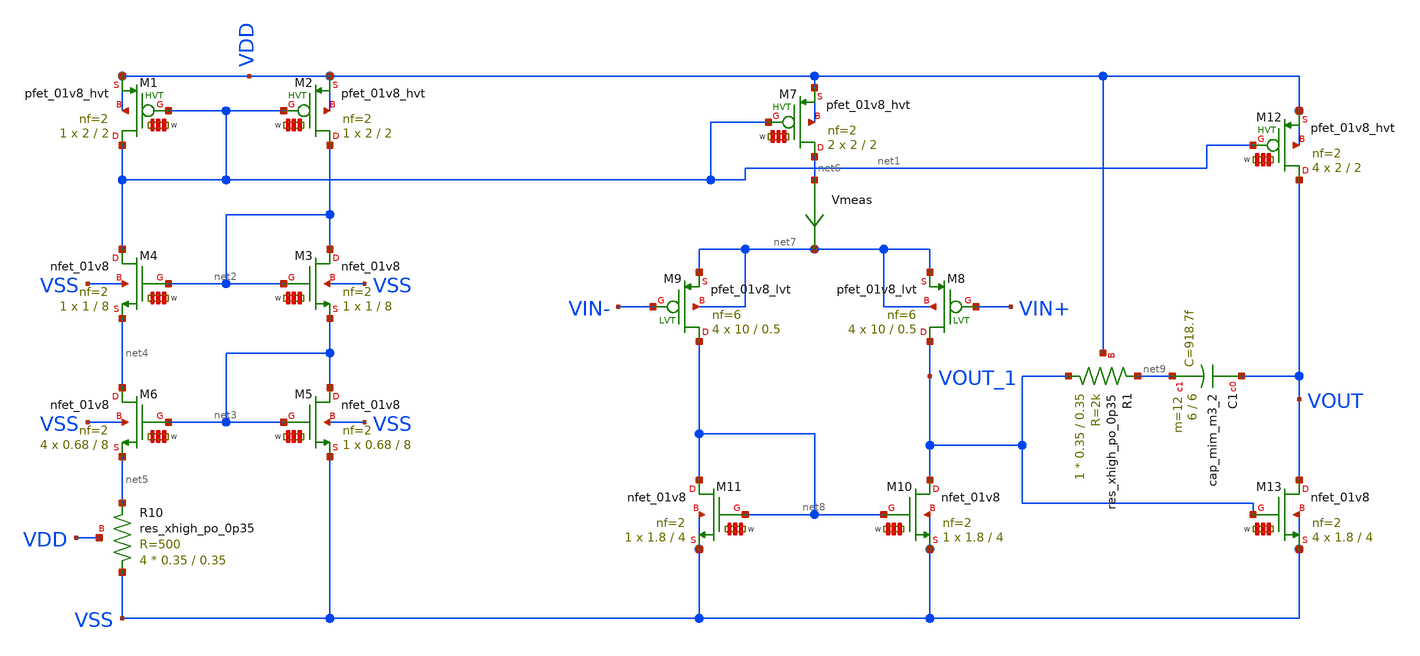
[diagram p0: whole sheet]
** sch_path: my_ip/sky130A/2_stage_op_amp_sky130/op_amp.sch
**.subckt op_amp
XM5 net3 net3 VSS VSS sky130_fd_pr__nfet_01v8 L=8 W='0.68 * 2 ' nf=2 ad='int((2 + 1)/2) * 0.68 / 2 * 0.29'
+ as='int((2 + 2)/2) * 0.68 / 2 * 0.29' pd='2*int((2 + 1)/2) * (0.68 / 2 + 0.29)' ps='2*int((2 + 2)/2) * (0.68 / 2 + 0.29)'
+ nrd='0.29 / 0.68 ' nrs='0.29 / 0.68 ' sa=0 sb=0 sd=0 mult=1 m=1
XM6 net4 net3 net5 VSS sky130_fd_pr__nfet_01v8 L=8 W='0.68 * 2 ' nf=2 ad='int((2 + 1)/2) * 0.68 / 2 * 0.29'
+ as='int((2 + 2)/2) * 0.68 / 2 * 0.29' pd='2*int((2 + 1)/2) * (0.68 / 2 + 0.29)' ps='2*int((2 + 2)/2) * (0.68 / 2 + 0.29)'
+ nrd='0.29 / 0.68 ' nrs='0.29 / 0.68 ' sa=0 sb=0 sd=0 mult=4 m=4
Vmeas net6 net7 0
.save i(vmeas)
XM7 net6 net1 VDD VDD sky130_fd_pr__pfet_01v8_hvt L=2 W='2 * 2 ' nf=2 ad='int((2 + 1)/2) * 2 / 2 * 0.29'
+ as='int((2 + 2)/2) * 2 / 2 * 0.29' pd='2*int((2 + 1)/2) * (2 / 2 + 0.29)' ps='2*int((2 + 2)/2) * (2 / 2 + 0.29)'
+ nrd='0.29 / 2 ' nrs='0.29 / 2 ' sa=0 sb=0 sd=0 mult=2 m=2
XM2 net2 net1 VDD VDD sky130_fd_pr__pfet_01v8_hvt L=2 W='2 * 2 ' nf=2 ad='int((2 + 1)/2) * 2 / 2 * 0.29'
+ as='int((2 + 2)/2) * 2 / 2 * 0.29' pd='2*int((2 + 1)/2) * (2 / 2 + 0.29)' ps='2*int((2 + 2)/2) * (2 / 2 + 0.29)'
+ nrd='0.29 / 2 ' nrs='0.29 / 2 ' sa=0 sb=0 sd=0 mult=1 m=1
XM1 net1 net1 VDD VDD sky130_fd_pr__pfet_01v8_hvt L=2 W='2 * 2 ' nf=2 ad='int((2 + 1)/2) * 2 / 2 * 0.29'
+ as='int((2 + 2)/2) * 2 / 2 * 0.29' pd='2*int((2 + 1)/2) * (2 / 2 + 0.29)' ps='2*int((2 + 2)/2) * (2 / 2 + 0.29)'
+ nrd='0.29 / 2 ' nrs='0.29 / 2 ' sa=0 sb=0 sd=0 mult=1 m=1
XR10 VSS net5 VDD sky130_fd_pr__res_xhigh_po_0p35 L=0.35 mult=4 m=4
XM4 net1 net2 net4 VSS sky130_fd_pr__nfet_01v8 L=8 W='1 * 2 ' nf=2 ad='int((2 + 1)/2) * 1 / 2 * 0.29'
+ as='int((2 + 2)/2) * 1 / 2 * 0.29' pd='2*int((2 + 1)/2) * (1 / 2 + 0.29)' ps='2*int((2 + 2)/2) * (1 / 2 + 0.29)'
+ nrd='0.29 / 1 ' nrs='0.29 / 1 ' sa=0 sb=0 sd=0 mult=1 m=1
XM3 net2 net2 net3 VSS sky130_fd_pr__nfet_01v8 L=8 W='1 * 2 ' nf=2 ad='int((2 + 1)/2) * 1 / 2 * 0.29'
+ as='int((2 + 2)/2) * 1 / 2 * 0.29' pd='2*int((2 + 1)/2) * (1 / 2 + 0.29)' ps='2*int((2 + 2)/2) * (1 / 2 + 0.29)'
+ nrd='0.29 / 1 ' nrs='0.29 / 1 ' sa=0 sb=0 sd=0 mult=1 m=1
XM8 VOUT_1 VIN+ net7 net7 sky130_fd_pr__pfet_01v8_lvt L=0.5 W=10 nf=6 ad='int((6 + 1)/2) * 10 / 6 * 0.29'
+ as='int((6 + 2)/2) * 10 / 6 * 0.29' pd='2*int((6 + 1)/2) * (10 / 6 + 0.29)' ps='2*int((6 + 2)/2) * (10 / 6 + 0.29)'
+ nrd='0.29 / 10 ' nrs='0.29 / 10 ' sa=0 sb=0 sd=0 mult=4 m=4
XM9 net8 VIN- net7 net7 sky130_fd_pr__pfet_01v8_lvt L=0.5 W=10 nf=6 ad='int((6 + 1)/2) * 10 / 6 * 0.29'
+ as='int((6 + 2)/2) * 10 / 6 * 0.29' pd='2*int((6 + 1)/2) * (10 / 6 + 0.29)' ps='2*int((6 + 2)/2) * (10 / 6 + 0.29)'
+ nrd='0.29 / 10 ' nrs='0.29 / 10 ' sa=0 sb=0 sd=0 mult=4 m=4
XM10 VOUT_1 net8 VSS VSS sky130_fd_pr__nfet_01v8 L=4 W='1.8 * 2 ' nf=2 ad='int((2 + 1)/2) * 1.8 / 2 * 0.29'
+ as='int((2 + 2)/2) * 1.8 / 2 * 0.29' pd='2*int((2 + 1)/2) * (1.8 / 2 + 0.29)' ps='2*int((2 + 2)/2) * (1.8 / 2 + 0.29)'
+ nrd='0.29 / 1.8 ' nrs='0.29 / 1.8 ' sa=0 sb=0 sd=0 mult=1 m=1
XM11 net8 net8 VSS VSS sky130_fd_pr__nfet_01v8 L=4 W='1.8 * 2 ' nf=2 ad='int((2 + 1)/2) * 1.8 / 2 * 0.29'
+ as='int((2 + 2)/2) * 1.8 / 2 * 0.29' pd='2*int((2 + 1)/2) * (1.8 / 2 + 0.29)' ps='2*int((2 + 2)/2) * (1.8 / 2 + 0.29)'
+ nrd='0.29 / 1.8 ' nrs='0.29 / 1.8 ' sa=0 sb=0 sd=0 mult=1 m=1
XM12 VOUT net1 VDD VDD sky130_fd_pr__pfet_01v8_hvt L=2 W='2 * 2 ' nf=2 ad='int((2 + 1)/2) * 2 / 2 * 0.29'
+ as='int((2 + 2)/2) * 2 / 2 * 0.29' pd='2*int((2 + 1)/2) * (2 / 2 + 0.29)' ps='2*int((2 + 2)/2) * (2 / 2 + 0.29)'
+ nrd='0.29 / 2 ' nrs='0.29 / 2 ' sa=0 sb=0 sd=0 mult=4 m=4
XM13 VOUT VOUT_1 VSS VSS sky130_fd_pr__nfet_01v8 L=4 W='1.8 * 2 ' nf=2 ad='int((2 + 1)/2) * 1.8 / 2 * 0.29'
+ as='int((2 + 2)/2) * 1.8 / 2 * 0.29' pd='2*int((2 + 1)/2) * (1.8 / 2 + 0.29)' ps='2*int((2 + 2)/2) * (1.8 / 2 + 0.29)'
+ nrd='0.29 / 1.8 ' nrs='0.29 / 1.8 ' sa=0 sb=0 sd=0 mult=4 m=4
XC1 VOUT net9 sky130_fd_pr__cap_mim_m3_2 W=6 L=6 MF=12 m=12
XR1 VOUT_1 net9 VDD sky130_fd_pr__res_xhigh_po_0p35 L=0.35 mult=1 m=1
**.ends
.end
